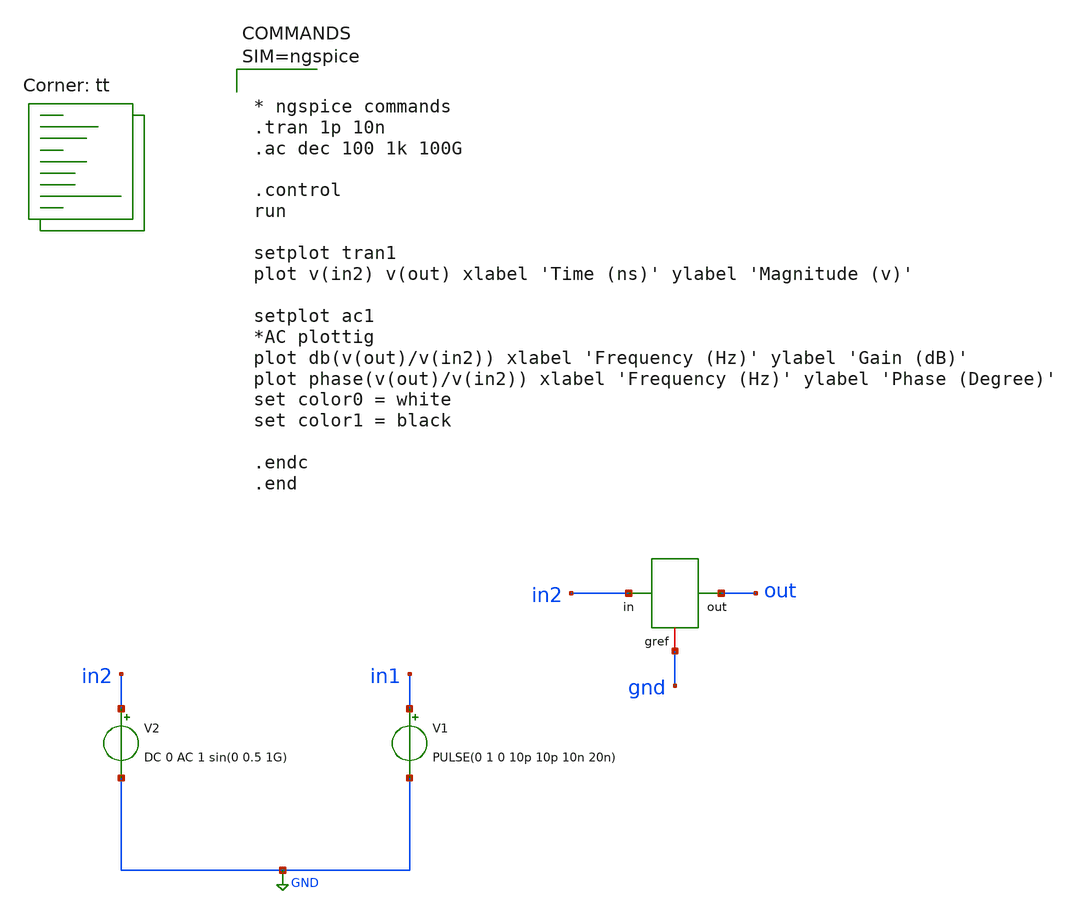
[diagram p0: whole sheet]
** sch_path: XSCHEM_DESIGNS/Filters/tb_FirstOrder_RC_Filter.sch
**.subckt tb_FirstOrder_RC_Filter
x1 out in2 gnd FirstOrder_RC_Filter
V1 in1 GND PULSE(0 1 0 10p 10p 10n 20n)
V2 in2 GND DC 0 AC 1 sin(0 0.5 1G)
**** begin user architecture code



* ngspice commands
.tran 1p 10n
.ac dec 100 1k 100G

.control
run

setplot tran1
plot v(in2) v(out) xlabel 'Time (ns)' ylabel 'Magnitude (v)'

setplot ac1
*AC plottig
plot db(v(out)/v(in2)) xlabel 'Frequency (Hz)' ylabel 'Gain (dB)'
plot phase(v(out)/v(in2)) xlabel 'Frequency (Hz)' ylabel 'Phase (Degree)'
set color0 = white
set color1 = black

.endc
.end



.lib $::SKYWATER_MODELS/sky130.lib.spice tt
**** end user architecture code
**.ends

* expanding   symbol:  FirstOrder_RC_Filter.sym # of pins=3
** sym_path: XSCHEM_DESIGNS/Filters/FirstOrder_RC_Filter.sym
** sch_path: XSCHEM_DESIGNS/Filters/FirstOrder_RC_Filter.sch
.subckt FirstOrder_RC_Filter out in gref
*.ipin in
*.opin out
*.iopin gref
R1 in out 1k m=1
C1 out gref 1p m=1
.ends

.GLOBAL GND
.end
